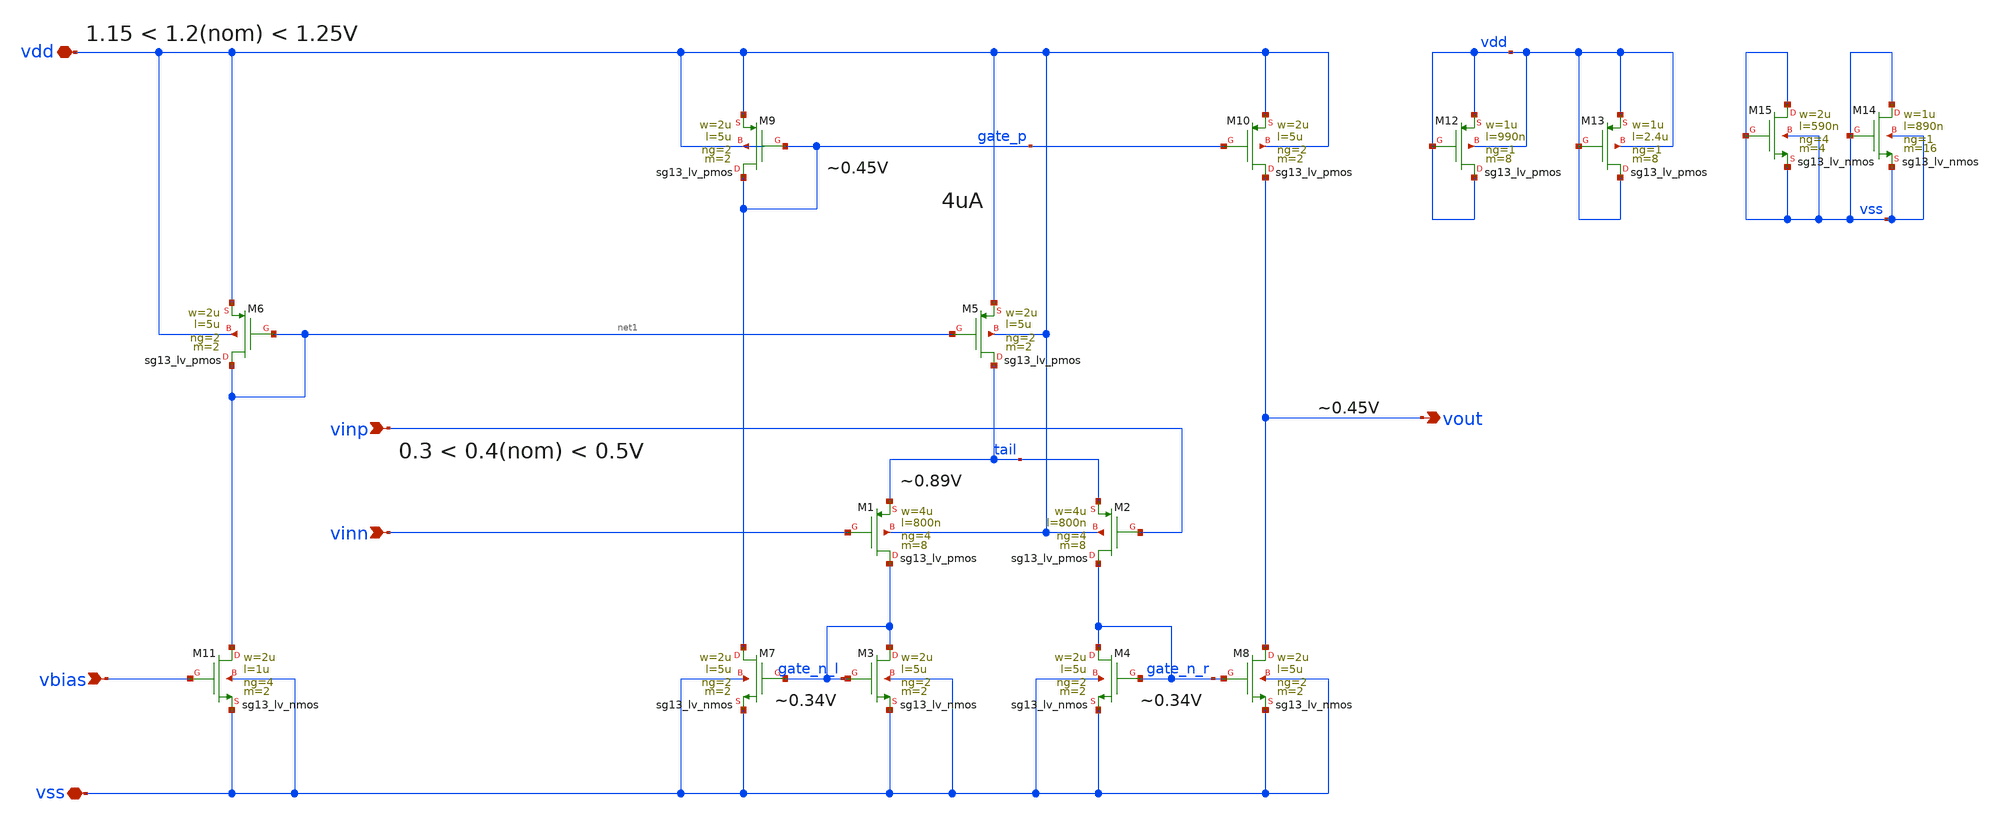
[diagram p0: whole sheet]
** sch_path: v2_feature_extr/a_buff.sch
* (c) 2026 Arianna Rubino, Apache-2.0 license
**.subckt a_buff vinp vinn vbias vdd vss vout
*.ipin vinp
*.ipin vinn
*.ipin vbias
*.iopin vdd
*.iopin vss
*.opin vout
XM3 gate_n_l gate_n_l vss vss sg13_lv_nmos w=2u l=5u ng=2 m=2 mm_ok=1
XM1 gate_n_l vinn tail vdd sg13_lv_pmos w=4u l=800n ng=4 m=8 mm_ok=1
XM2 gate_n_r vinp tail vdd sg13_lv_pmos w=4u l=800n ng=4 m=8 mm_ok=1
XM5 tail net1 vdd vdd sg13_lv_pmos w=2u l=5u ng=2 m=2 mm_ok=1
XM4 gate_n_r gate_n_r vss vss sg13_lv_nmos w=2u l=5u ng=2 m=2 mm_ok=1
XM9 gate_p gate_p vdd vdd sg13_lv_pmos w=2u l=5u ng=2 m=2 mm_ok=1
XM10 vout gate_p vdd vdd sg13_lv_pmos w=2u l=5u ng=2 m=2 mm_ok=1
XM7 gate_p gate_n_l vss vss sg13_lv_nmos w=2u l=5u ng=2 m=2 mm_ok=1
XM8 vout gate_n_r vss vss sg13_lv_nmos w=2u l=5u ng=2 m=2 mm_ok=1
XM6 net1 net1 vdd vdd sg13_lv_pmos w=2u l=5u ng=2 m=2 mm_ok=1
XM11 net1 vbias vss vss sg13_lv_nmos w=2u l=1u ng=4 m=2 mm_ok=1
XM12 vdd vdd vdd vdd sg13_lv_pmos w=1u l=990n ng=1 m=8 mm_ok=1
XM13 vdd vdd vdd vdd sg13_lv_pmos w=1u l=2.4u ng=1 m=8 mm_ok=1
XM14 vss vss vss vss sg13_lv_nmos w=1u l=890n ng=1 m=16 mm_ok=1
XM15 vss vss vss vss sg13_lv_nmos w=2u l=590n ng=4 m=4 mm_ok=1
**.ends
.end
